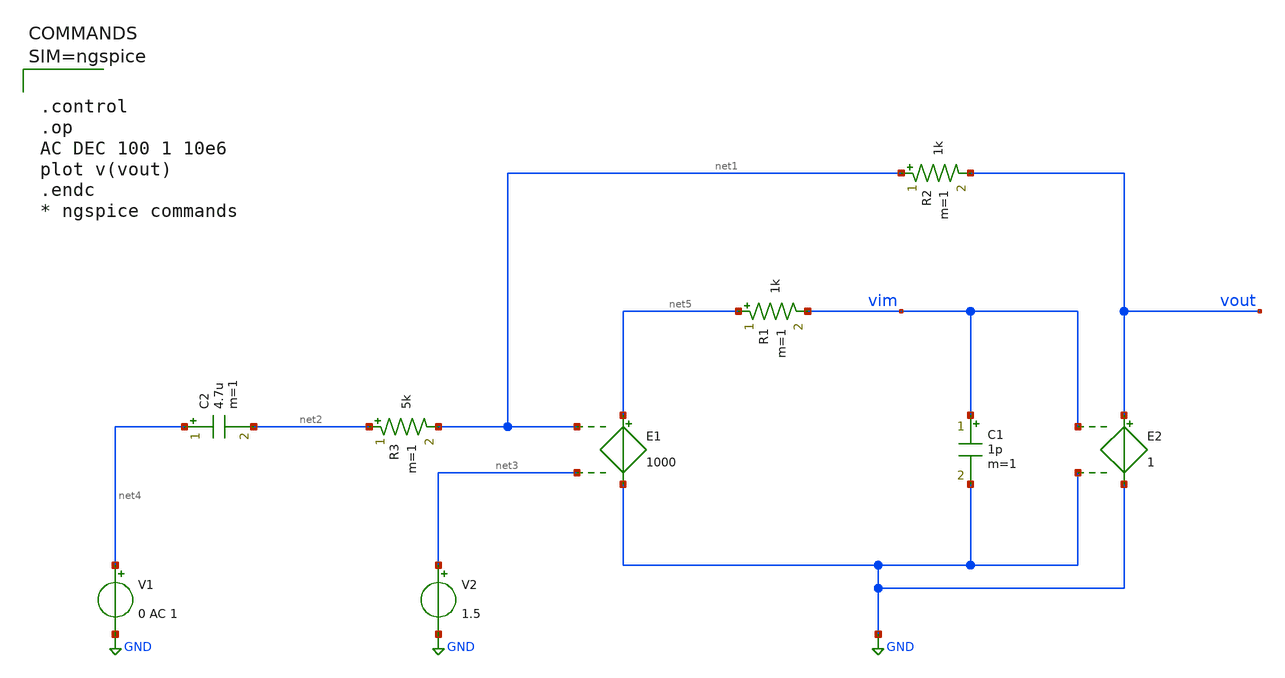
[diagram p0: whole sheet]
** sch_path: xschem/firstordermodel.sch
**.subckt firstordermodel
E1 net5 GND net1 net3 1000
E2 vout GND vim GND 1
R1 net5 vim 1k m=1
R2 net1 vout 1k m=1
C1 vim GND 1p m=1
R3 net2 net1 5k m=1
C2 net4 net2 4.7u m=1
V1 net4 GND 0 AC 1
V2 net3 GND 1.5
**** begin user architecture code



.control
.op
AC DEC 100 1 10e6
plot v(vout)
.endc
* ngspice commands



**** end user architecture code
**.ends
.GLOBAL GND
.end
